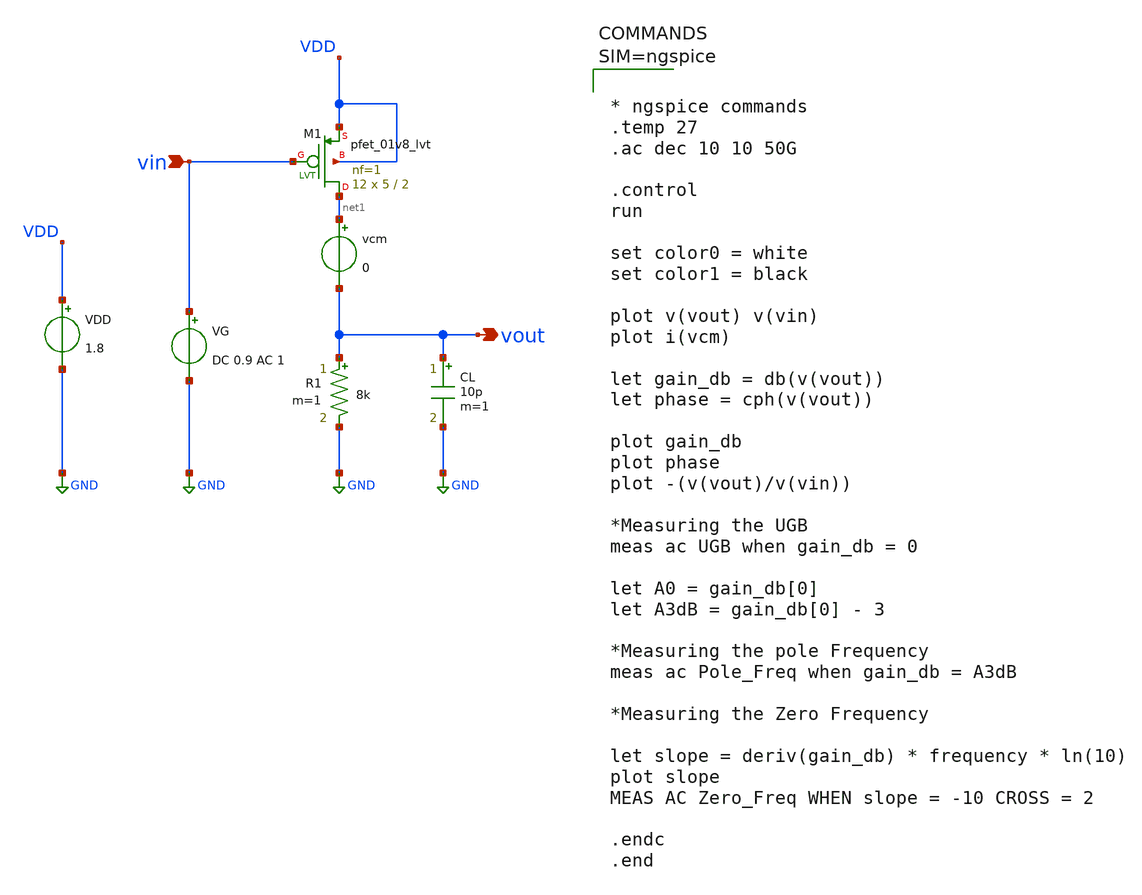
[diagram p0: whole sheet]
** sch_path: Common_Source_PMOS_Restitive_ckts/CS_Amp_PMOS_Restitive_Load_AC_Analysis.sch
**.subckt CS_Amp_PMOS_Restitive_Load_AC_Analysis vout vin
*.opin vout
*.ipin vin
R1 vout GND 8k m=1
CL vout GND 10p m=1
VG vin GND DC 0.9 AC 1
VDD VDD GND 1.8
vcm net1 vout 0
XM1 net1 vin VDD VDD sky130_fd_pr__pfet_01v8_lvt L=2 W=5 nf=1 ad='int((1 + 1)/2) * 5 / 1 * 0.29' as='int((1 + 2)/2) * 5 / 1 * 0.29'
+ pd='2*int((1 + 1)/2) * (5 / 1 + 0.29)' ps='2*int((1 + 2)/2) * (5 / 1 + 0.29)' nrd='0.29 / 5 ' nrs='0.29 / 5 '
+ sa=0 sb=0 sd=0 mult=12 m=12
**** begin user architecture code



* ngspice commands
.temp 27
.ac dec 10 10 50G

.control
run

set color0 = white
set color1 = black

plot v(vout) v(vin)
plot i(vcm)

let gain_db = db(v(vout))
let phase = cph(v(vout))

plot gain_db
plot phase
plot -(v(vout)/v(vin))

*Measuring the UGB
meas ac UGB when gain_db = 0

let A0 = gain_db[0]
let A3dB = gain_db[0] - 3

*Measuring the pole Frequency
meas ac Pole_Freq when gain_db = A3dB

*Measuring the Zero Frequency

let slope = deriv(gain_db) * frequency * ln(10)
plot slope
MEAS AC Zero_Freq WHEN slope = -10 CROSS = 2

.endc
.end





** opencircuitdesign pdks install
.lib $::SKYWATER_MODELS/sky130.lib.spice tt

**** end user architecture code
**.ends
.GLOBAL GND
.end
